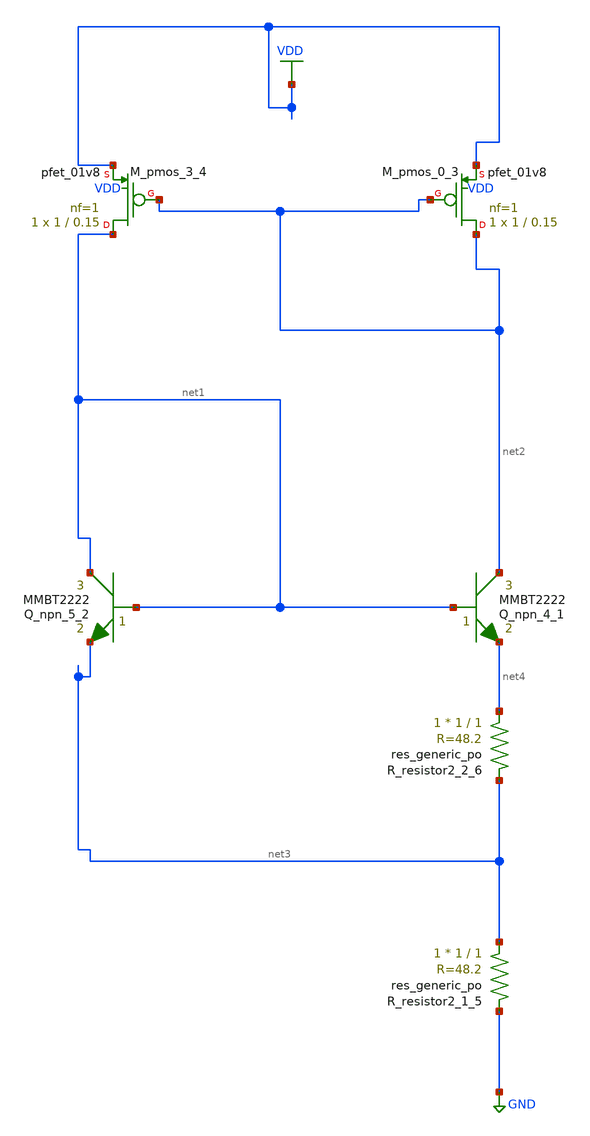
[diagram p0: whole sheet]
** sch_path: schematics/Image2Net/014.sch
**.subckt 014
Q_npn_4_1 net2 net1 net4 MMBT2222 area=1 m=1
Q_npn_5_2 net1 net1 net3 MMBT2222 area=1 m=1
XM_pmos_0_3 net2 net2 VDD VDD sky130_fd_pr__pfet_01v8 L=0.15 W=1 nf=1 ad='int((1 + 1)/2) * 1 / 1 * 0.29'
+ as='int((1 + 2)/2) * 1 / 1 * 0.29' pd='2*int((1 + 1)/2) * (1 / 1 + 0.29)' ps='2*int((1 + 2)/2) * (1 / 1 + 0.29)'
+ nrd='0.29 / 1 ' nrs='0.29 / 1 ' sa=0 sb=0 sd=0 mult=1 m=1
XM_pmos_3_4 net1 net2 VDD VDD sky130_fd_pr__pfet_01v8 L=0.15 W=1 nf=1 ad='int((1 + 1)/2) * 1 / 1 * 0.29'
+ as='int((1 + 2)/2) * 1 / 1 * 0.29' pd='2*int((1 + 1)/2) * (1 / 1 + 0.29)' ps='2*int((1 + 2)/2) * (1 / 1 + 0.29)'
+ nrd='0.29 / 1 ' nrs='0.29 / 1 ' sa=0 sb=0 sd=0 mult=1 m=1
XR_resistor2_1_5 net3 GND sky130_fd_pr__res_generic_po W=1 L=1 m=1
XR_resistor2_2_6 net4 net3 sky130_fd_pr__res_generic_po W=1 L=1 m=1
**.ends
.GLOBAL GND
.GLOBAL VDD
.end
